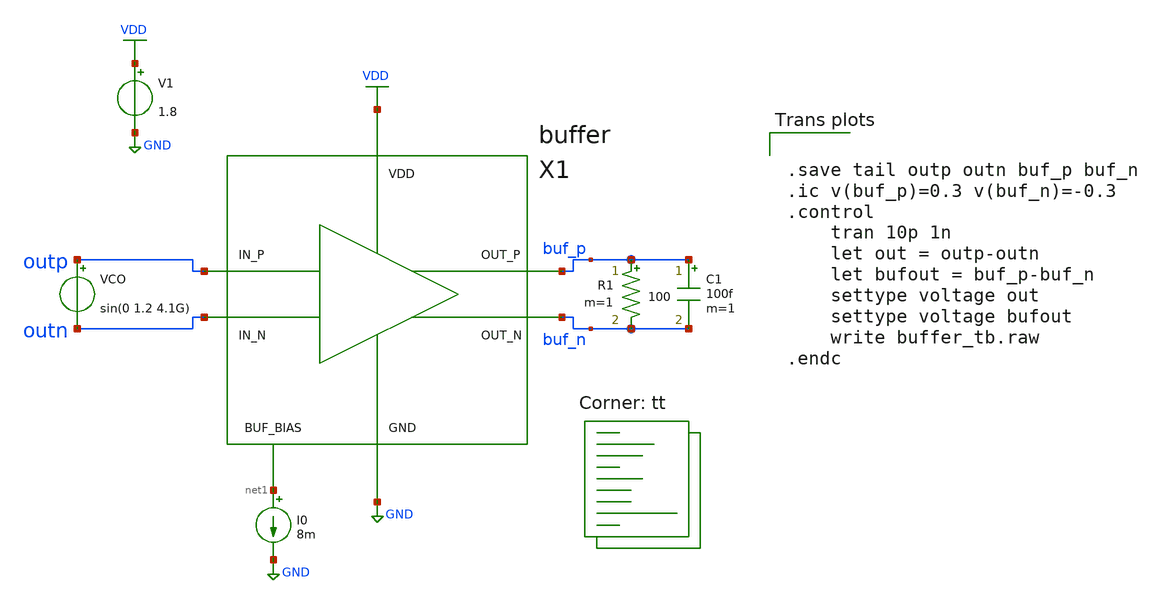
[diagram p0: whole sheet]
** sch_path: xschem/vco/testbenches/buffer/buffer_tb.sch
* YI/C9Shc8z/CWPKLJb8BQD+O4ziO4wpAwbu7u7s7HEAy2IIt2IIlQD6O4ziO4ypAAICtDl/GPL8AgNZy7Go7vwAAAAAAAAAAAAAAAAAAAAAAAPeMn2NHvywNosQhFFq
**.subckt buffer_tb
X1 net1 VDD GND buf_n buf_p outp outn buffer
R1 buf_p buf_n 100 m=1
C1 buf_p buf_n 100f m=1
V1 VDD GND 1.8
I0 net1 GND 8m
VCO outp outn sin(0 1.2 4.1G)
**** begin user architecture code


.save tail outp outn buf_p buf_n
.ic v(buf_p)=0.3 v(buf_n)=-0.3
.control
    tran 10p 1n
    let out = outp-outn
    let bufout = buf_p-buf_n
    settype voltage out
    settype voltage bufout
    write buffer_tb.raw
.endc


.lib $::SKYWATER_MODELS/sky130.lib.spice tt
**** end user architecture code
**.ends
.GLOBAL VDD
.GLOBAL GND
.end
